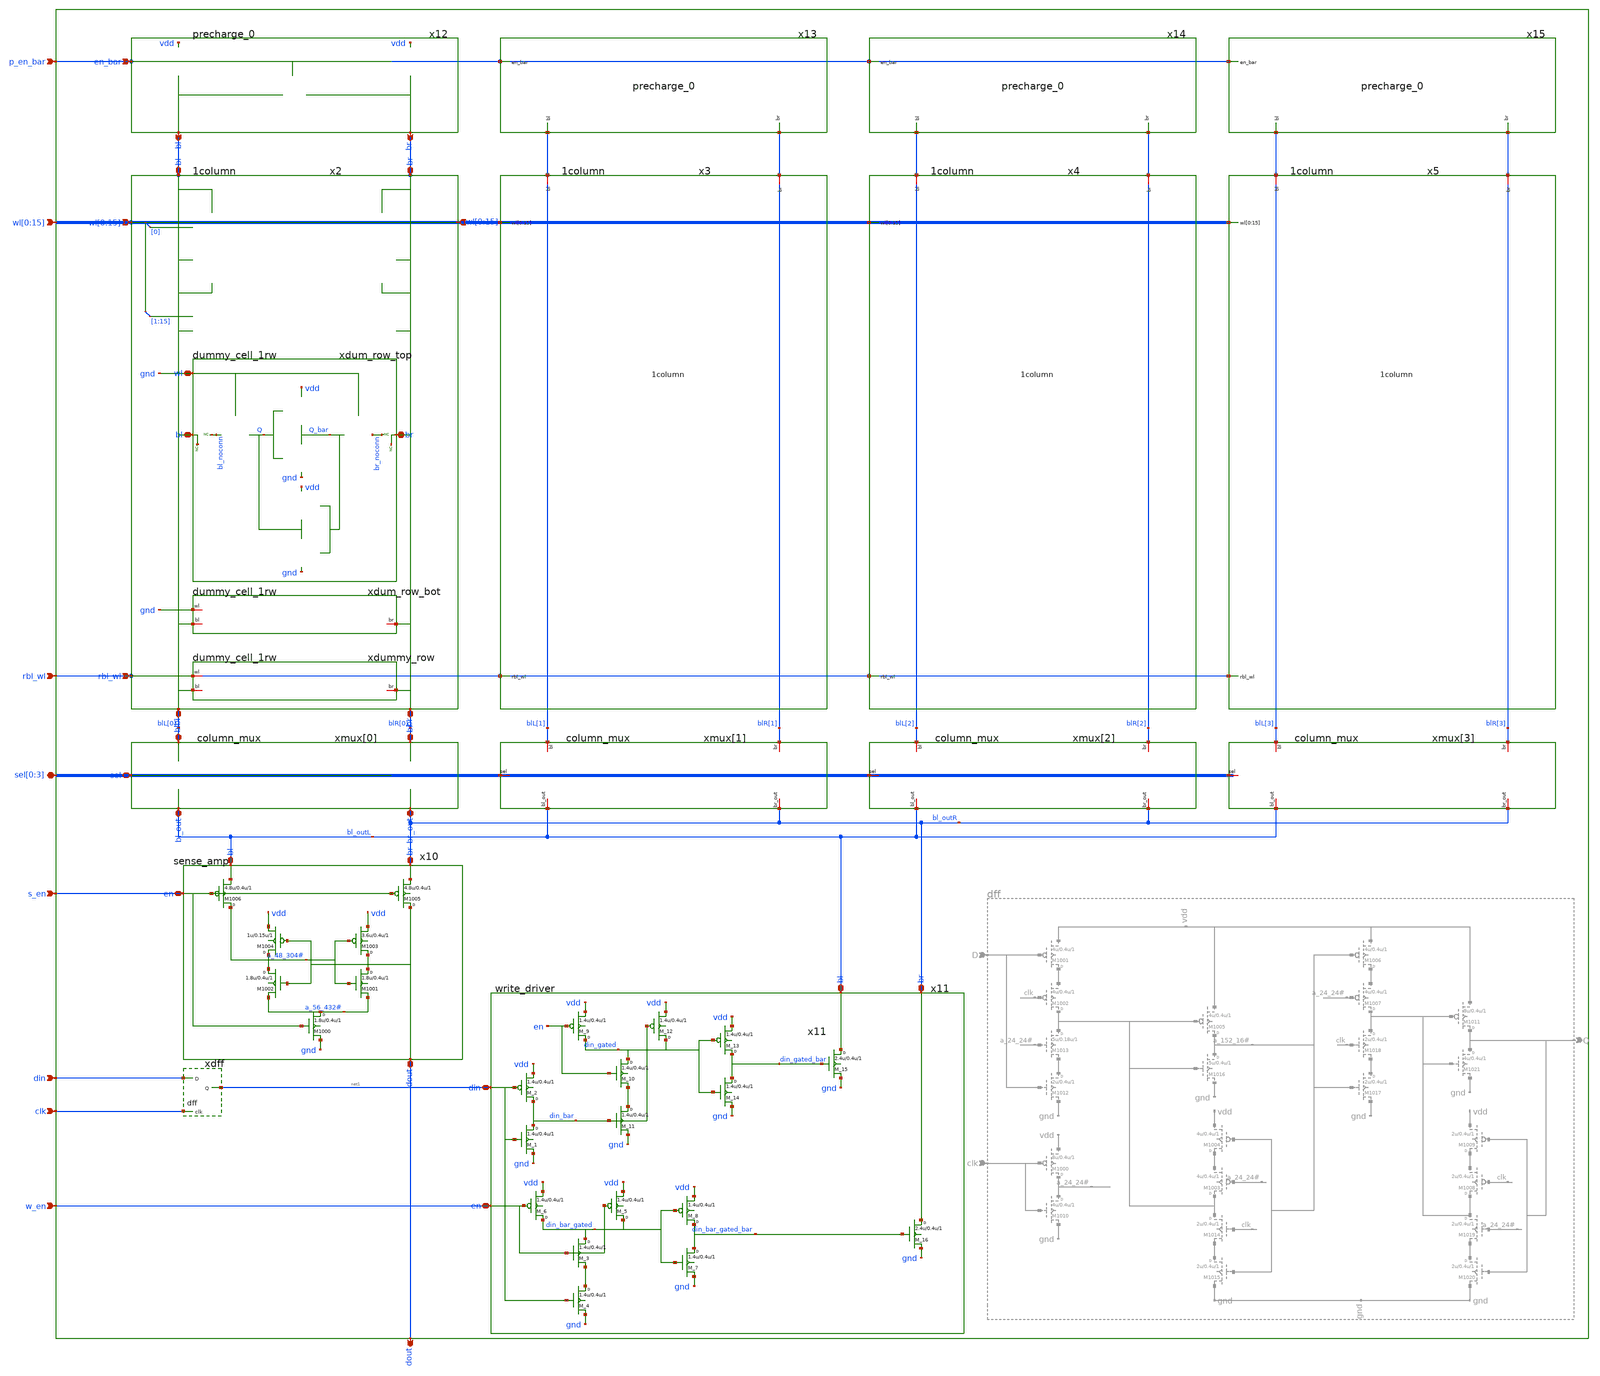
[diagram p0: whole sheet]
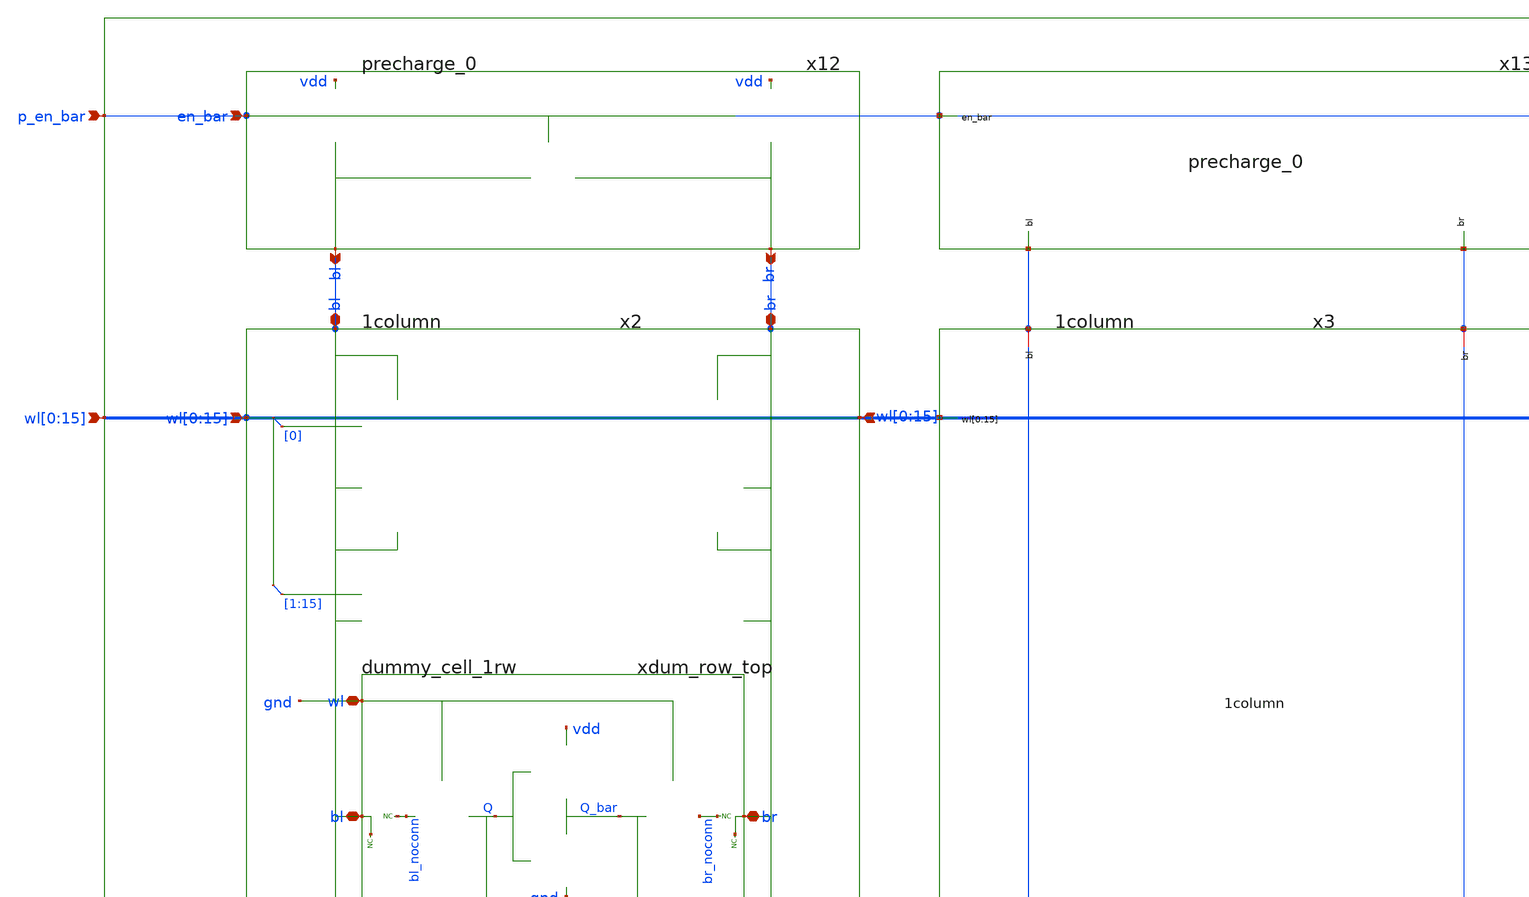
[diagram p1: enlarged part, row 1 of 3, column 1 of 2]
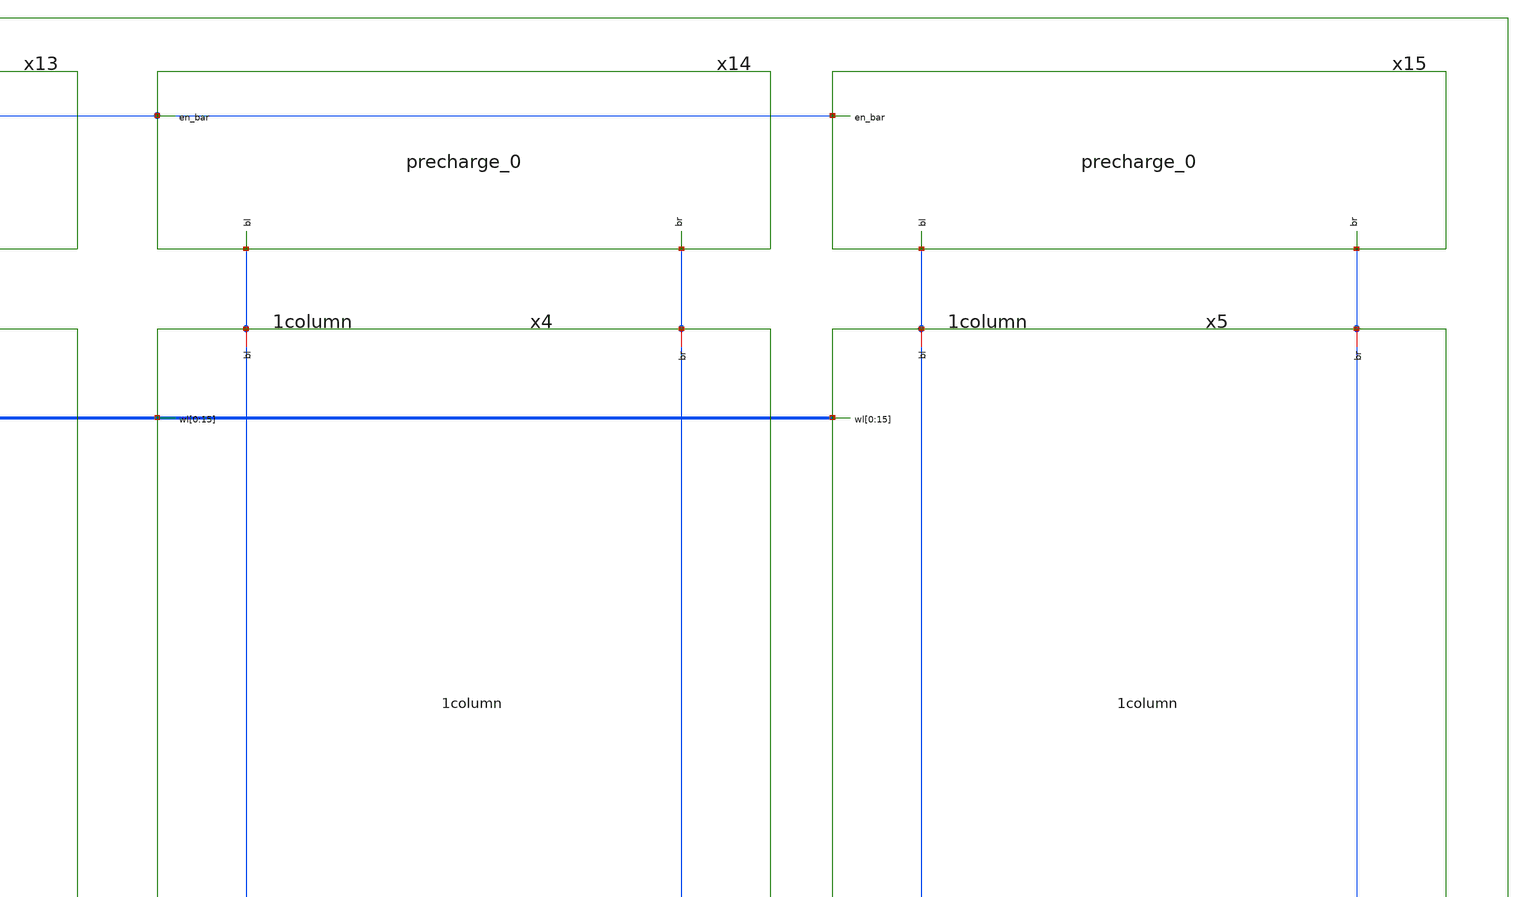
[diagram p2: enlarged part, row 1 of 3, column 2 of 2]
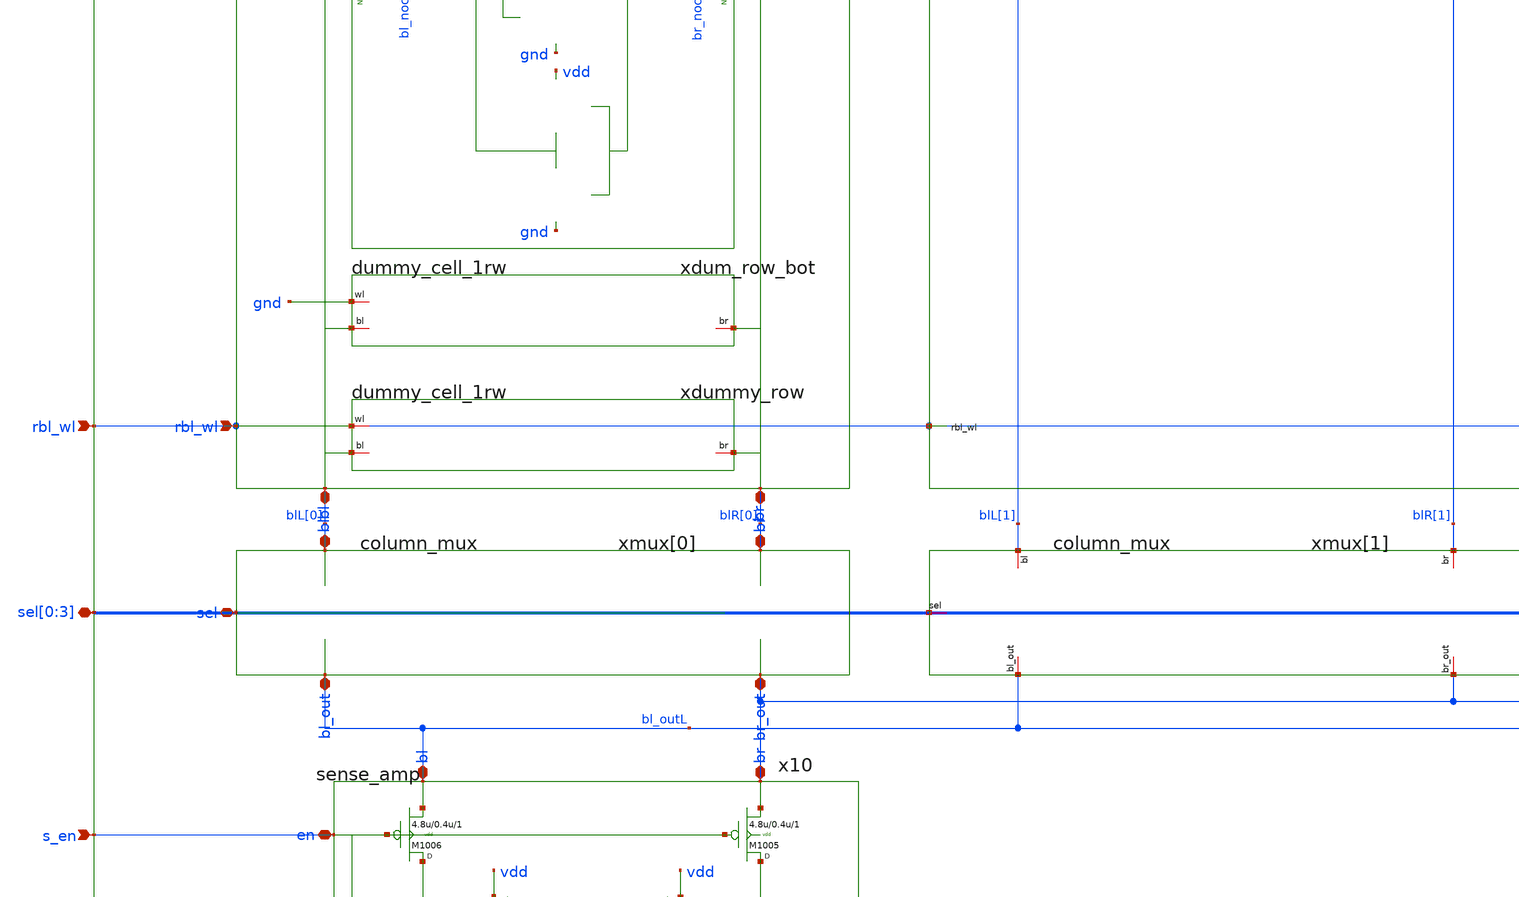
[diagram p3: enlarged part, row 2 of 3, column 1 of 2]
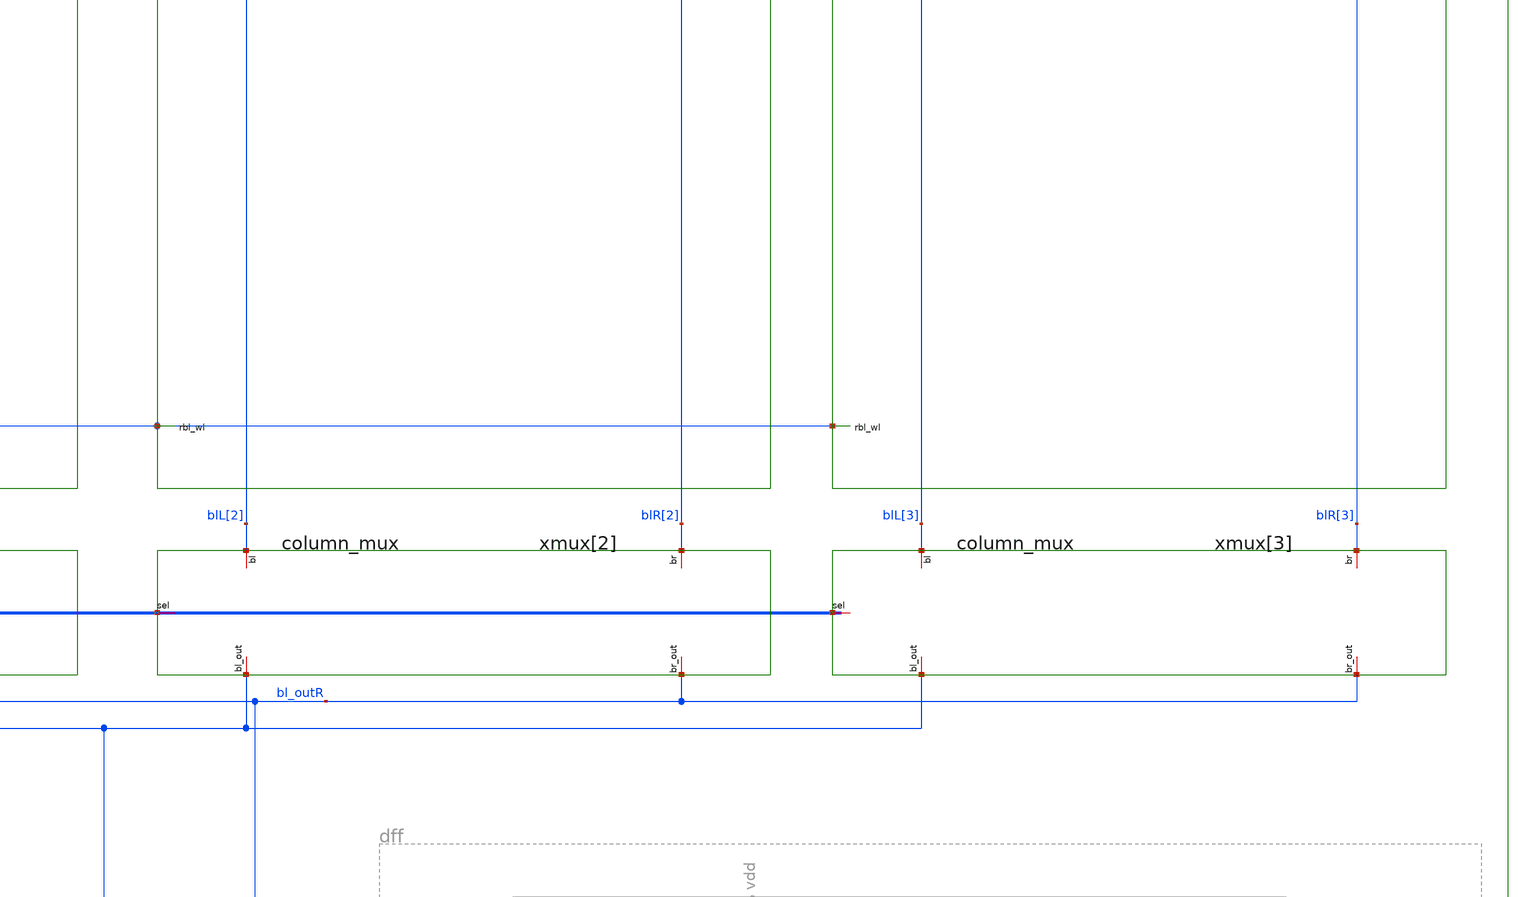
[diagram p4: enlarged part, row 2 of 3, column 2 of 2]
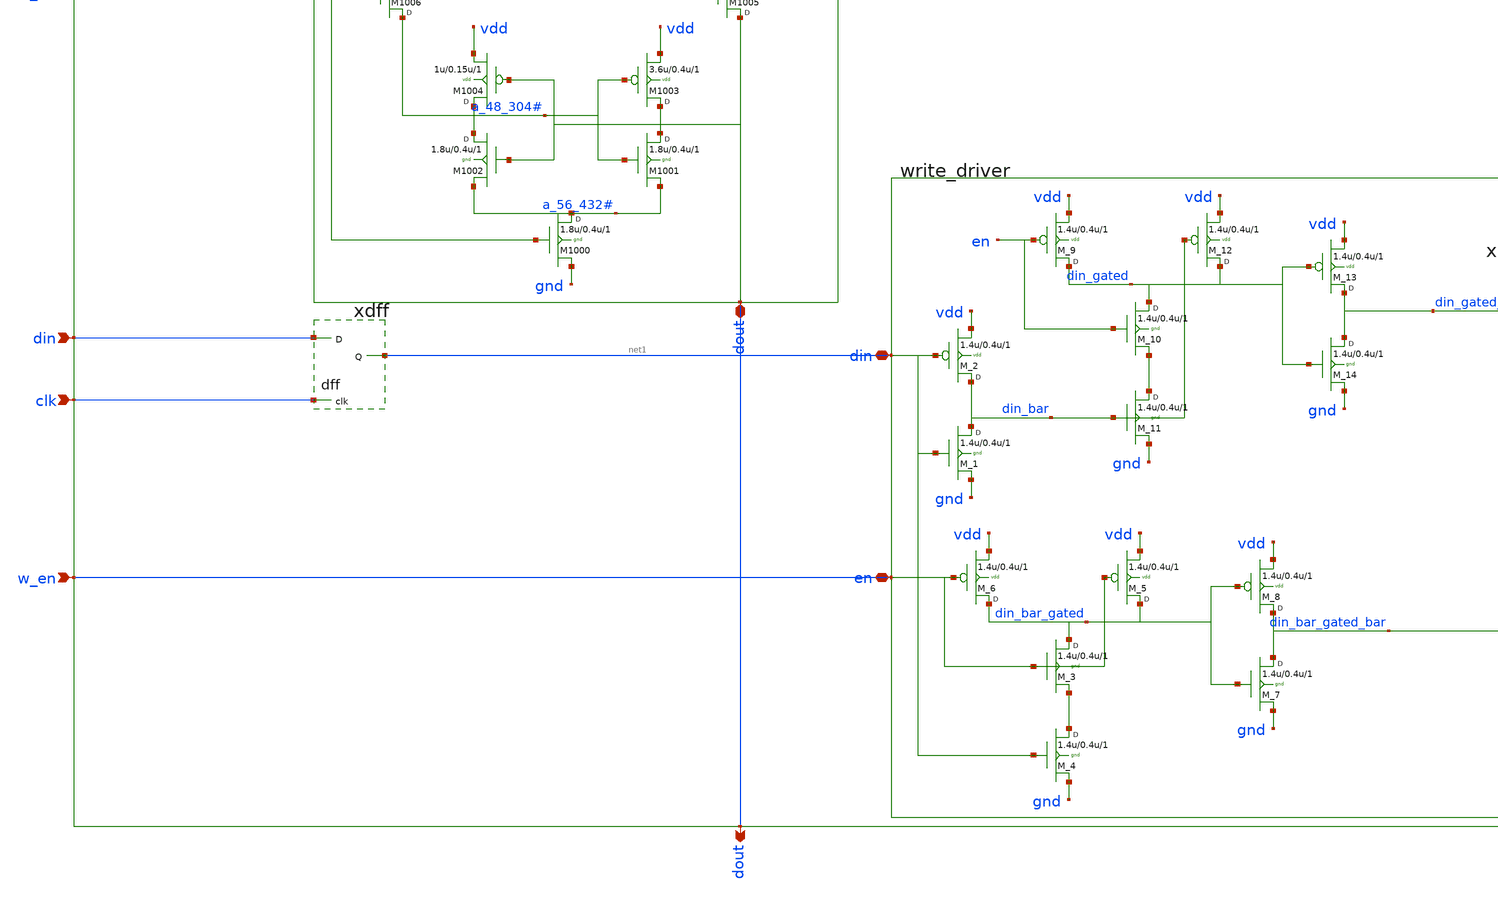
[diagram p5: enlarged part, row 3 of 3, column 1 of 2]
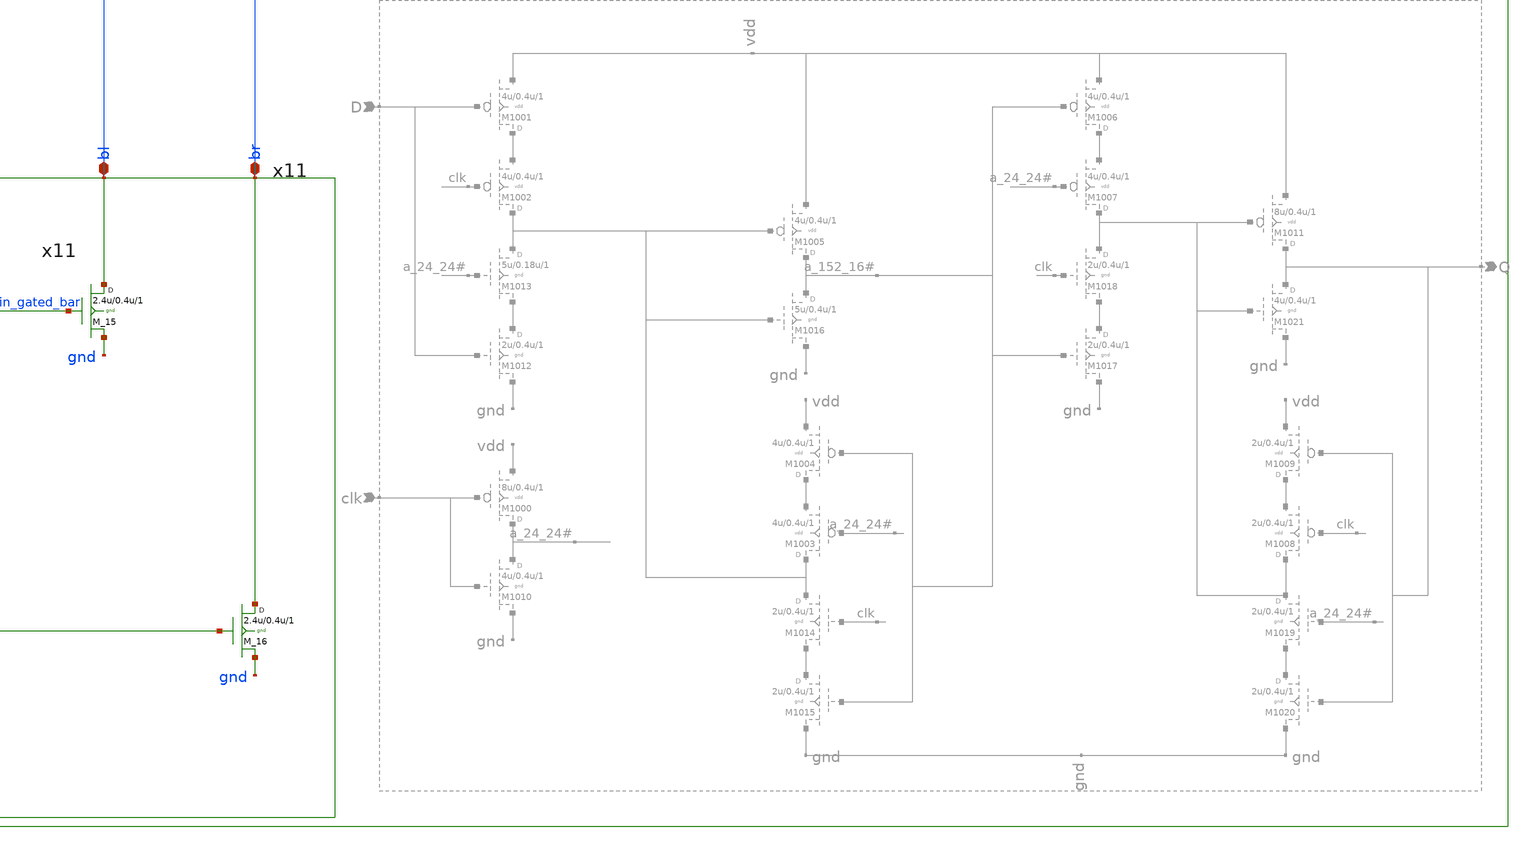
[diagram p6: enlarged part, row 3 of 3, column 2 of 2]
** sch_path: sram_2_64_scn4m_lcc/column.sch
**.subckt column dout din s_en p_en_bar w_en sel[0],sel[1],sel[2],sel[3]
*+ wl[0],wl[1],wl[2],wl[3],wl[4],wl[5],wl[6],wl[7],wl[8],wl[9],wl[10],wl[11],wl[12],wl[13],wl[14],wl[15] rbl_wl clk
*.opin dout
*.ipin din
*.ipin s_en
*.ipin p_en_bar
*.ipin w_en
*.iopin sel[0],sel[1],sel[2],sel[3]
*.ipin
*+ wl[0],wl[1],wl[2],wl[3],wl[4],wl[5],wl[6],wl[7],wl[8],wl[9],wl[10],wl[11],wl[12],wl[13],wl[14],wl[15]
*.ipin rbl_wl
*.ipin clk
x2 blL[0] blR[0] rbl_wl wl[0] wl[1] wl[2] wl[3] wl[4] wl[5] wl[6] wl[7] wl[8] wl[9] wl[10] wl[11]
+ wl[12] wl[13] wl[14] wl[15] vdd gnd 1column
x4 blR[2] blL[2] wl[0] wl[1] wl[2] wl[3] wl[4] wl[5] wl[6] wl[7] wl[8] wl[9] wl[10] wl[11] wl[12]
+ wl[13] wl[14] wl[15] rbl_wl vdd gnd 1column
x5 blR[3] blL[3] wl[0] wl[1] wl[2] wl[3] wl[4] wl[5] wl[6] wl[7] wl[8] wl[9] wl[10] wl[11] wl[12]
+ wl[13] wl[14] wl[15] rbl_wl vdd gnd 1column
xmux[0] blL[0] blR[0] sel[0] bl_outL bl_outR vdd gnd column_mux
xmux[1] blL[1] blR[1] sel[0] bl_outL bl_outR vdd gnd column_mux
xmux[2] blL[2] blR[2] sel[0] bl_outL bl_outR vdd gnd column_mux
xmux[3] blL[3] blR[3] sel[0] bl_outL bl_outR vdd gnd column_mux
x10 bl_outL bl_outR dout s_en vdd gnd sense_amp
x11 net1 bl_outL bl_outR w_en vdd gnd write_driver
x12 blL[0] blR[0] p_en_bar vdd precharge_0
x13 blL[1] blR[1] p_en_bar vdd precharge_0
x14 blL[2] blR[2] p_en_bar vdd precharge_0
x15 blL[3] blR[3] p_en_bar vdd precharge_0
xdff din net1 clk vdd gnd dff
x3 blR[1] blL[1] wl[0] wl[1] wl[2] wl[3] wl[4] wl[5] wl[6] wl[7] wl[8] wl[9] wl[10] wl[11] wl[12]
+ wl[13] wl[14] wl[15] rbl_wl vdd gnd 1column
**.ends
.end
